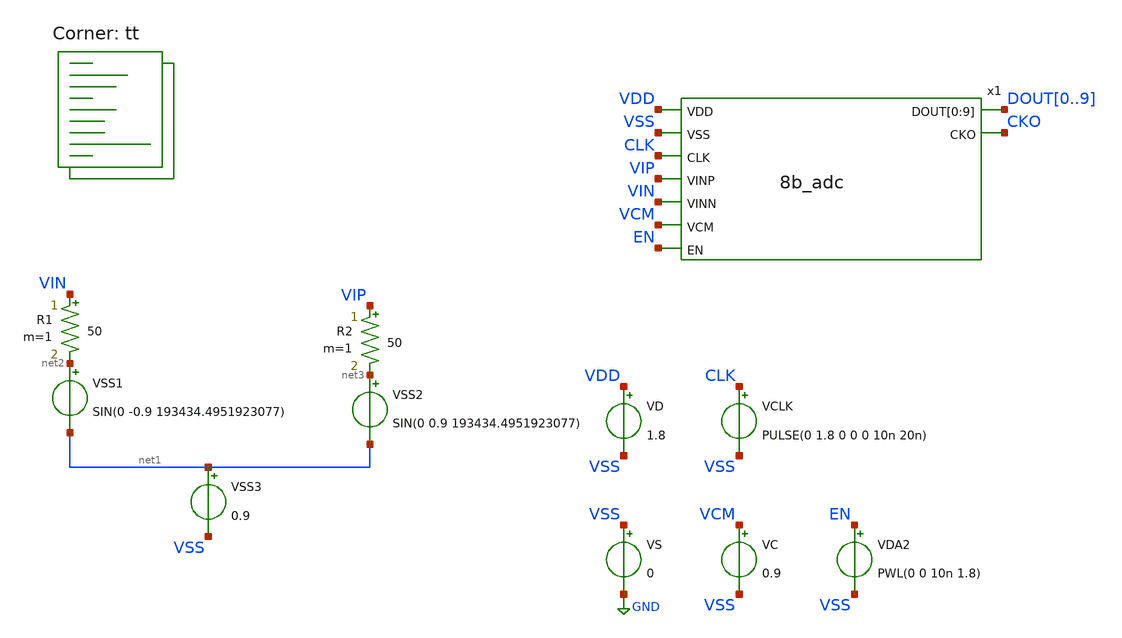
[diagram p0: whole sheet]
** sch_path: xschem/adc_tb.sch
**.subckt adc_tb
VS VSS GND 0
VD VDD VSS 1.8
VSS1 net2 net1 SIN(0 -0.9 193434.4951923077)
VSS2 net3 net1 SIN(0 0.9 193434.4951923077)
VSS3 net1 VSS 0.9
VCLK CLK VSS PULSE(0 1.8 0 0 0 10n 20n)
R1 VIN net2 50 m=1
R2 VIP net3 50 m=1
x1 VDD VSS CLK VIP VIN VCM EN DOUT0 DOUT1 DOUT2 DOUT3 DOUT4 DOUT5 DOUT6 DOUT7 DOUT8 DOUT9 CKO 8b_adc
VC VCM VSS 0.9
VDA2 EN VSS PWL(0 0 10n 1.8)
**** begin user architecture code

** opencircuitdesign pdks install
* .lib $::SKYWATER_MODELS/sky130.lib.spice tt
*.include $PDK_ROOT/$PDK/libs.ref/sky130_fd_sc_hdll/spice/sky130_fd_sc_hdll.spice
.include $PDK_ROOT/$PDK/libs.ref/sky130_fd_sc_hs/spice/sky130_fd_sc_hs.spice
*.include $PDK_ROOT/$PDK/libs.ref/sky130_fd_sc_hd/spice/sky130_fd_sc_hd.spice



.option wnflag=0 bypass=1
.options method=gear rawfile=binary
.options solver=klu nomod
.control
global netlist_dir .
set num_threads=32
set wr_singlescale
save x1.vcp x1.vcn vip vin clk vcm cko x1.cks x1.cksb vdd i(vd)  dout0 dout1 dout2 dout3 dout4 dout5
+ dout6 dout7 dout8 dout9
tran 1n 535u 0 0.1n uic ; Mengubah start time menjadi 10n
rusage traniter trantime
let pow = -i(vd)*vdd
meas tran inst_pow MAX pow from=1n to=535u
meas tran avg_pow  AVG pow from=1n to=535u
remzerovec
write adc10b_tb_dynamic.raw
wrdata adc10b_tb_dynamic.txt cko dout0 dout1 dout2 dout3 dout4 dout5 dout6 dout7 dout8 dout9 pow
quit 1
.endc


.lib $::SKYWATER_MODELS/sky130.lib.spice tt
**** end user architecture code
**.ends
.GLOBAL GND
.end
